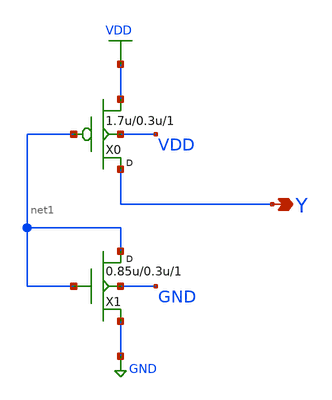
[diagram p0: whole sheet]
** sch_path: openfasoc/common/platforms/gf180osu9t/lib/tiehi/gf180mcu_osu_sc_tiehi.sch
**.subckt gf180mcu_osu_sc_tiehi Y
*.opin Y
X0 Y net1 VDD VDD pmos_3p3 w=1.7u l=0.3u m=1
X1 net1 net1 GND GND nmos_3p3 w=0.85u l=0.3u m=1
**.ends
.GLOBAL VDD
.GLOBAL GND
.end
